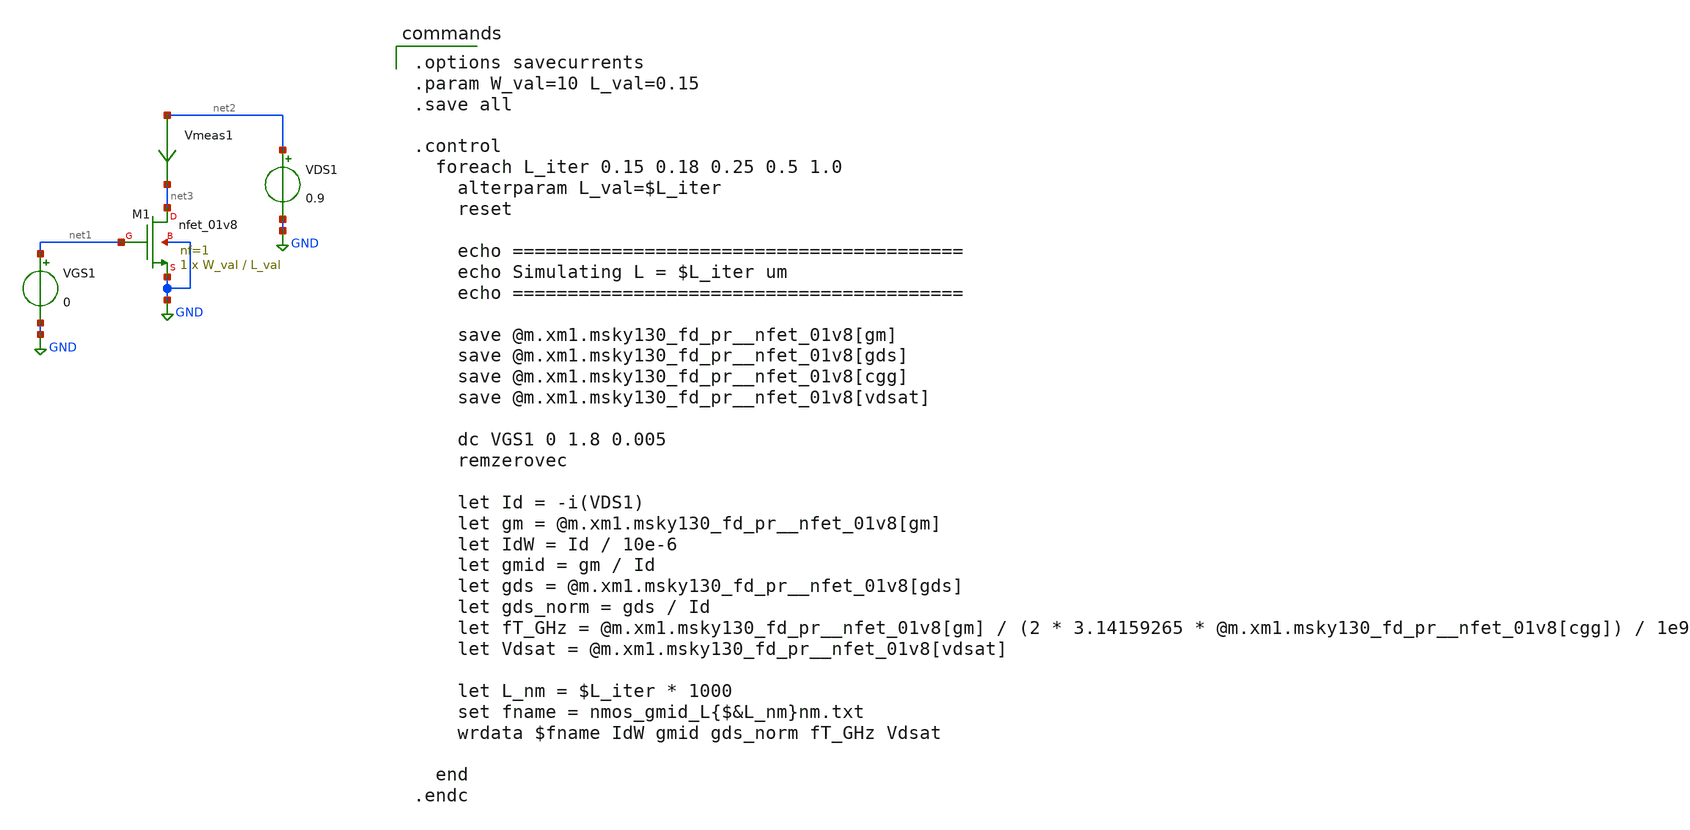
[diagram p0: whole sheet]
** sch_path: 01_xschem_ngspice/soluzioni/lab02/xschem/nmos_gmid.sch
**.subckt nmos_gmid
XM1 net3 net1 GND GND sky130_fd_pr__nfet_01v8 L=L_val W=W_val nf=1 ad='int((1 + 1)/2) * W_val / 1 * 0.29'
+ as='int((1 + 2)/2) * W_val / 1 * 0.29' pd='2*int((1 + 1)/2) * (W_val / 1 + 0.29)' ps='2*int((1 + 2)/2) * (W_val / 1 + 0.29)'
+ nrd='0.29 / W_val ' nrs='0.29 / W_val ' sa=0 sb=0 sd=0 mult=1 m=1
VGS1 net1 GND 0
VDS1 net2 GND 0.9
Vmeas1 net2 net3 0
.save i(vmeas1)
**** begin user architecture code

** opencircuitdesign pdks install
.lib $::SKYWATER_MODELS/sky130.lib.spice tt


.options savecurrents
.param W_val=10 L_val=0.15
.save all

.control
  foreach L_iter 0.15 0.18 0.25 0.5 1.0
    alterparam L_val=$L_iter
    reset

    echo =========================================
    echo Simulating L = $L_iter um
    echo =========================================

    save @m.xm1.msky130_fd_pr__nfet_01v8[gm]
    save @m.xm1.msky130_fd_pr__nfet_01v8[gds]
    save @m.xm1.msky130_fd_pr__nfet_01v8[cgg]
    save @m.xm1.msky130_fd_pr__nfet_01v8[vdsat]

    dc VGS1 0 1.8 0.005
    remzerovec

    let Id = -i(VDS1)
    let gm = @m.xm1.msky130_fd_pr__nfet_01v8[gm]
    let IdW = Id / 10e-6
    let gmid = gm / Id
    let gds = @m.xm1.msky130_fd_pr__nfet_01v8[gds]
    let gds_norm = gds / Id
    let fT_GHz = @m.xm1.msky130_fd_pr__nfet_01v8[gm] / (2 * 3.14159265 *
+ @m.xm1.msky130_fd_pr__nfet_01v8[cgg]) / 1e9
    let Vdsat = @m.xm1.msky130_fd_pr__nfet_01v8[vdsat]

    let L_nm = $L_iter * 1000
    set fname = nmos_gmid_L{$&L_nm}nm.txt
    wrdata $fname IdW gmid gds_norm fT_GHz Vdsat

  end
.endc

**** end user architecture code
**.ends
.GLOBAL GND
.end
